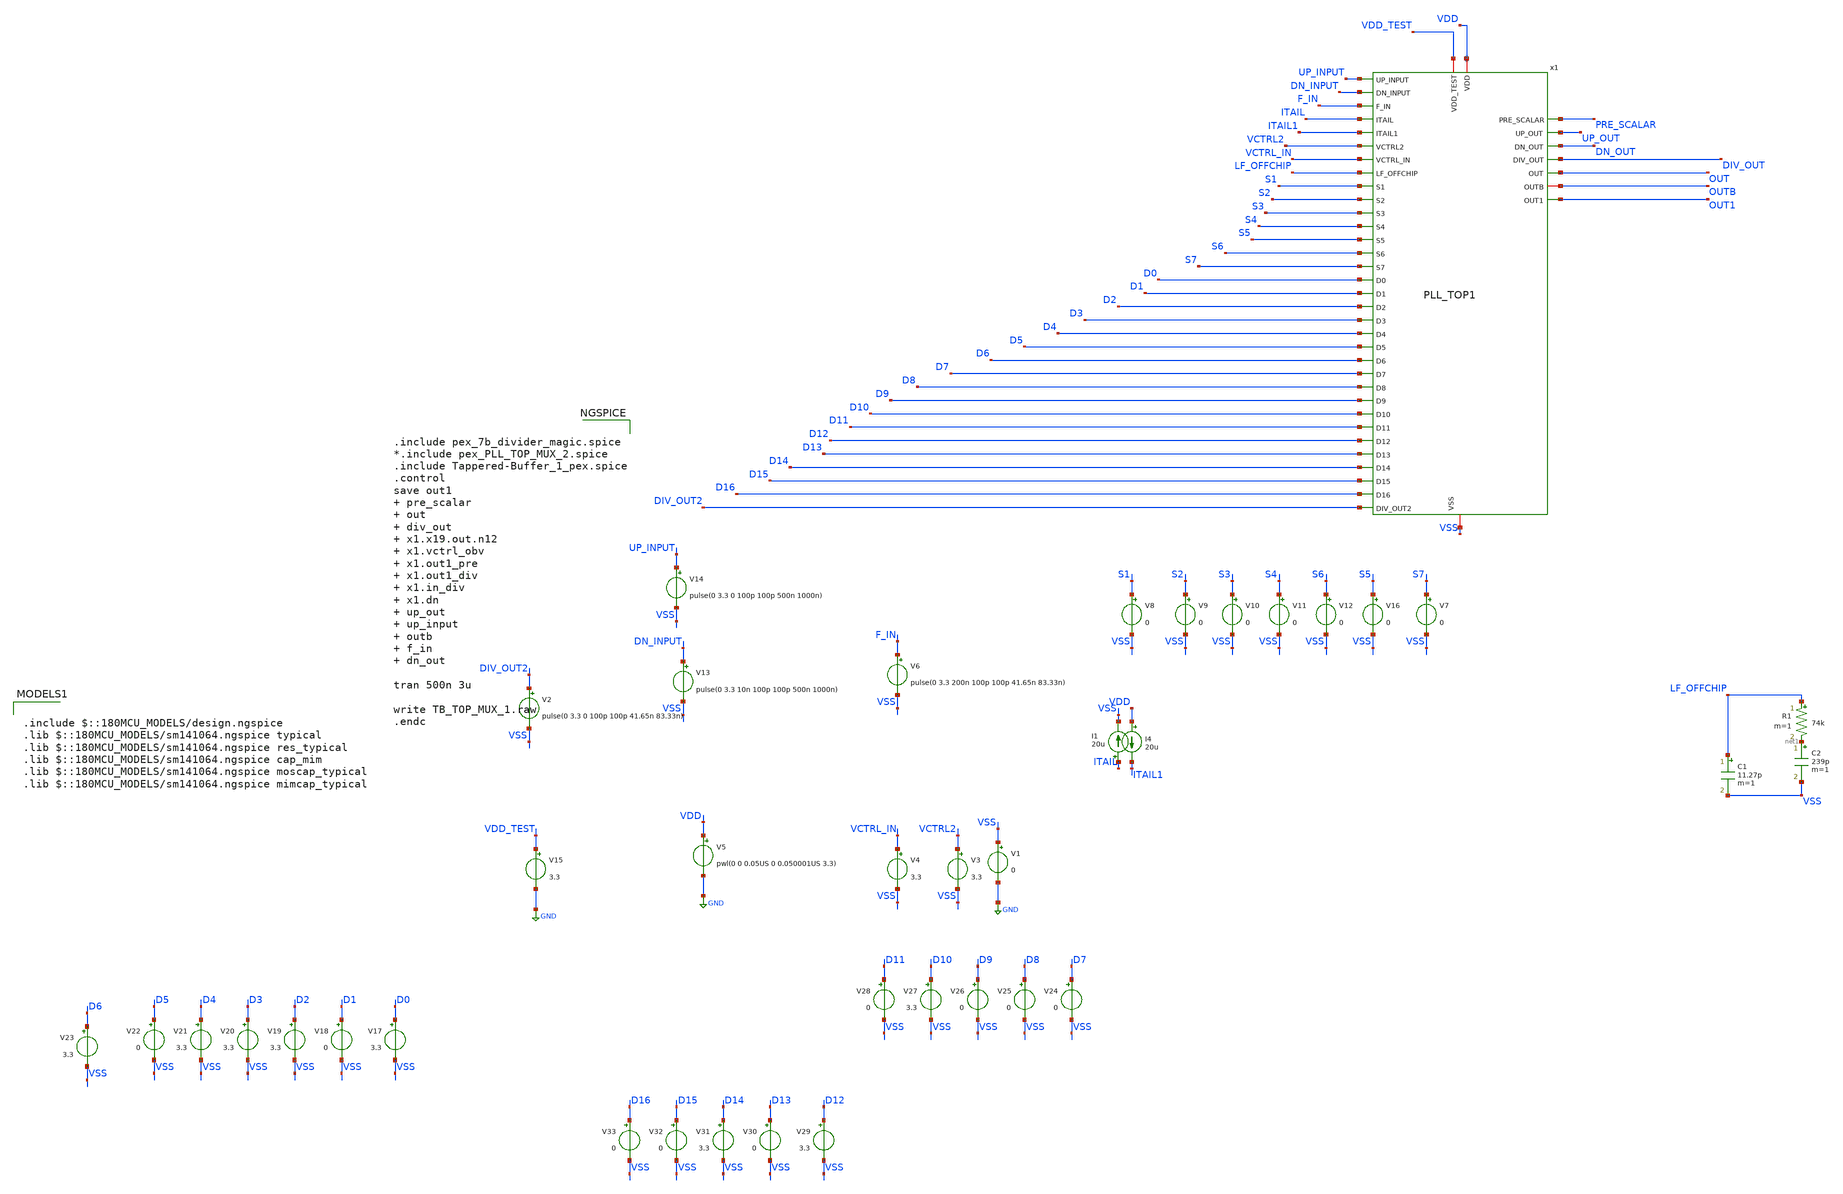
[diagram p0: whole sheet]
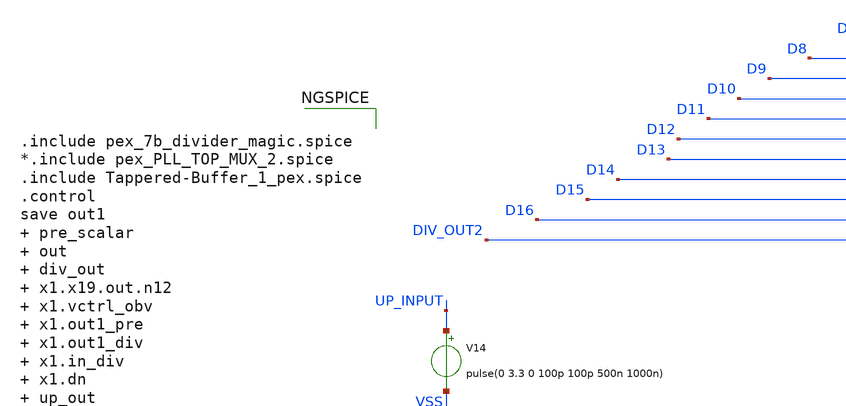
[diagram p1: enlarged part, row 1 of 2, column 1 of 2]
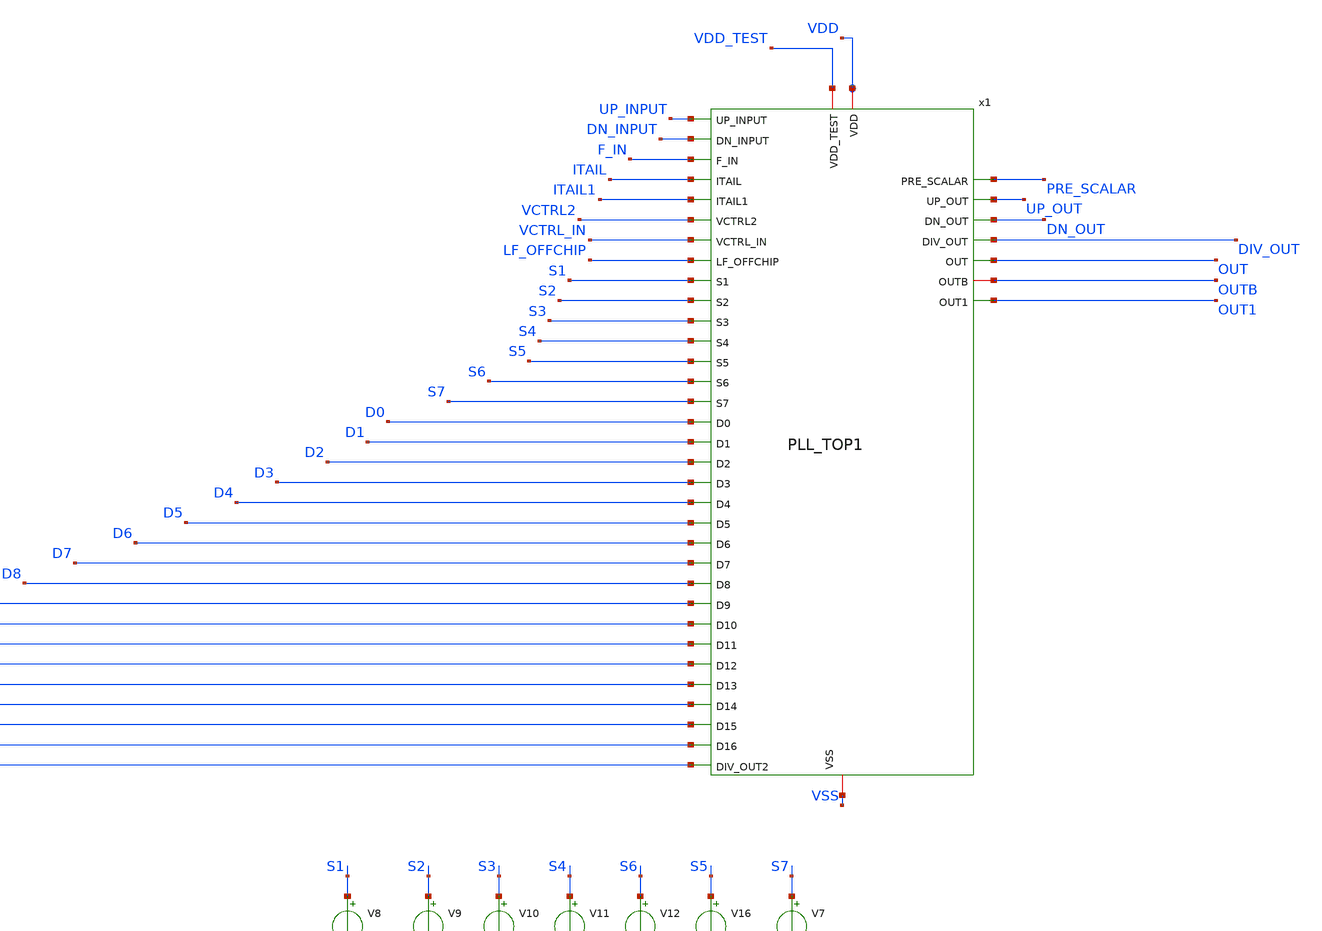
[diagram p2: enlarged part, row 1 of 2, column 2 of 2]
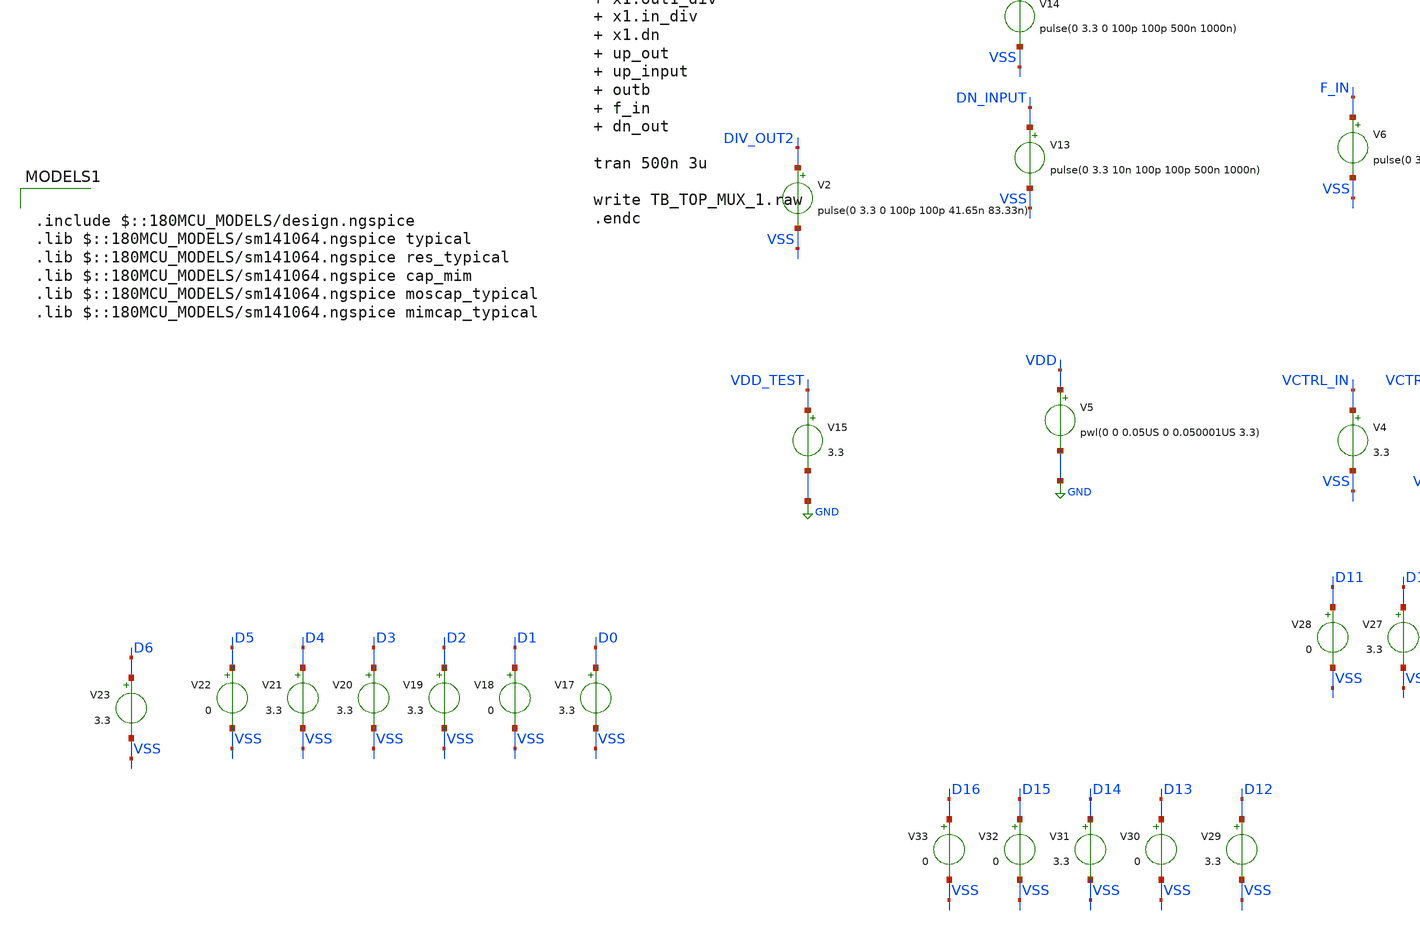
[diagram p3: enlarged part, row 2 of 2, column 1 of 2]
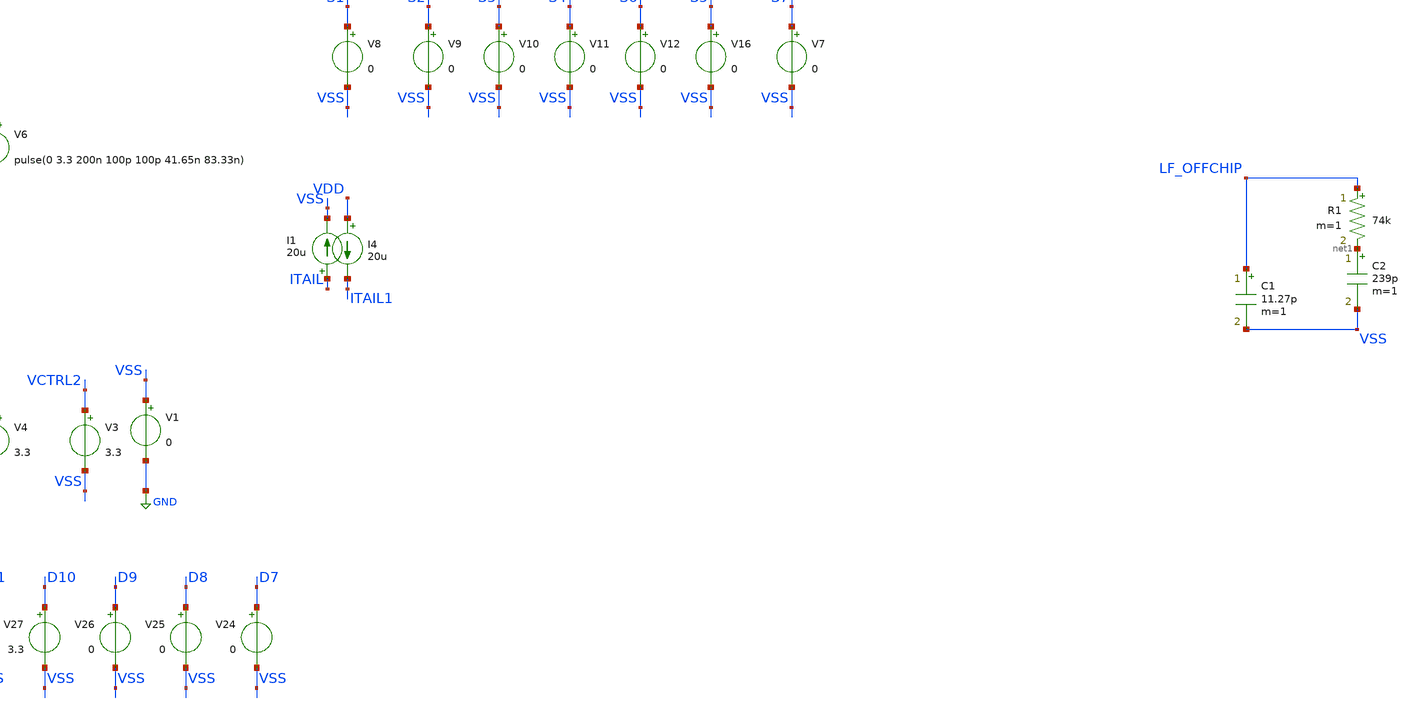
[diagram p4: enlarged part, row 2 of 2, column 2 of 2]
** sch_path: Clock_Generator_PAKISTAN_06/Xschem/TB_TOP_MUX_1.sch
**.subckt TB_TOP_MUX_1
V1 VSS GND 0
V3 VCTRL2 VSS 3.3
V4 VCTRL_IN VSS 3.3
V6 F_IN VSS pulse(0 3.3 200n 100p 100p 41.65n 83.33n)
I1 ITAIL VSS 20u
I4 VDD ITAIL1 20u
V8 S1 VSS 0
V9 S2 VSS 0
V10 S3 VSS 0
V11 S4 VSS 0
V12 S6 VSS 0
V13 DN_INPUT VSS pulse(0 3.3 10n 100p 100p 500n 1000n)
V14 UP_INPUT VSS pulse(0 3.3 0 100p 100p 500n 1000n)
V15 VDD_TEST GND 3.3
C1 LF_OFFCHIP VSS 11.27p m=1
R1 LF_OFFCHIP net1 74k m=1
C2 net1 VSS 239p m=1
V16 S5 VSS 0
x1 VDD_TEST D12 D0 UP_INPUT VDD D13 D1 DN_INPUT VSS D14 D2 PRE_SCALAR UP_OUT D15 D3 F_IN DN_OUT D16
+ D4 ITAIL DIV_OUT D5 ITAIL1 S1 D6 VCTRL_IN S6 D7 VCTRL2 S2 D8 OUT S3 S4 OUTB D9 S5 D10 LF_OFFCHIP S7
+ D11 OUT1 DIV_OUT2 PLL_TOP1
V17 D0 VSS 3.3
V18 D1 VSS 0
V19 D2 VSS 3.3
V20 D3 VSS 3.3
V21 D4 VSS 3.3
V22 D5 VSS 0
V23 D6 VSS 3.3
V24 D7 VSS 0
V25 D8 VSS 0
V26 D9 VSS 0
V27 D10 VSS 3.3
V28 D11 VSS 0
V29 D12 VSS 3.3
V30 D13 VSS 0
V31 D14 VSS 3.3
V32 D15 VSS 0
V33 D16 VSS 0
V5 VDD GND pwl(0 0 0.05US 0 0.050001US 3.3)
V2 DIV_OUT2 VSS pulse(0 3.3 0 100p 100p 41.65n 83.33n)
V7 S7 VSS 0
**** begin user architecture code


.include pex_7b_divider_magic.spice
*.include pex_PLL_TOP_MUX_2.spice
.include Tappered-Buffer_1_pex.spice
.control
save out1  pre_scalar  out  div_out  x1.x19.out.n12  x1.vctrl_obv  x1.out1_pre  x1.out1_div
+  x1.in_div  x1.dn  up_out  up_input  outb  f_in  dn_out

tran 500n 3u

write TB_TOP_MUX_1.raw
.endc



.include $::180MCU_MODELS/design.ngspice
.lib $::180MCU_MODELS/sm141064.ngspice typical
.lib $::180MCU_MODELS/sm141064.ngspice res_typical
.lib $::180MCU_MODELS/sm141064.ngspice cap_mim
.lib $::180MCU_MODELS/sm141064.ngspice moscap_typical
.lib $::180MCU_MODELS/sm141064.ngspice mimcap_typical

**** end user architecture code
**.ends
.GLOBAL GND
.end
